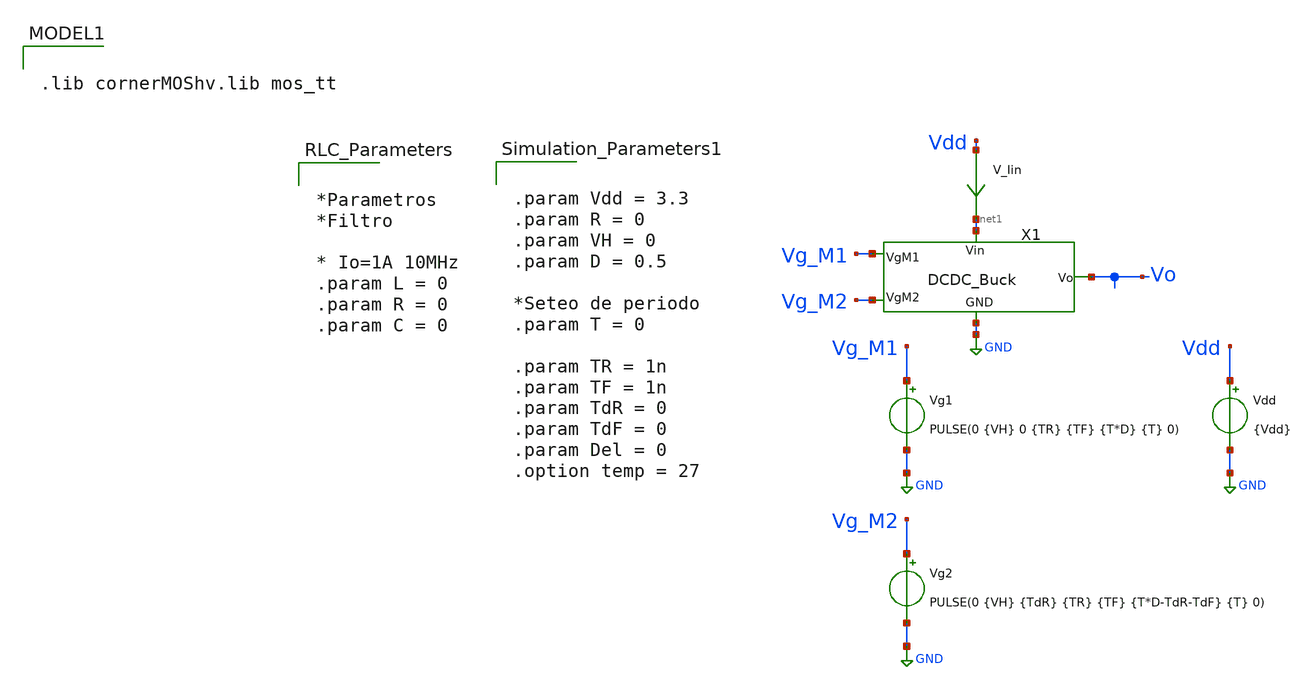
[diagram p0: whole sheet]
** sch_path: ChipUSM_AnalogTrack24/DCDCBuck/TB_DCDCBuck.sch
**.subckt TB_DCDCBuck
Vdd Vdd GND {Vdd}
Vg2 Vg_M2 GND PULSE(0 {VH} {TdR} {TR} {TF} {T*D-TdR-TdF} {T} 0)
Vg1 Vg_M1 GND PULSE(0 {VH} 0 {TR} {TF} {T*D} {T} 0)
V_Iin Vdd net1 0
.save i(v_iin)
X1 Vg_M1 Vg_M2 GND net1 Vo DCDC_Buck
**** begin user architecture code

.lib cornerMOShv.lib mos_tt



*Parametros
*Filtro

* Io=1A 10MHz
.param L = 0
.param R = 0
.param C = 0





.save all  @n.x1.xm1.nsg13_hv_pmos[ids]  @n.x1.xm2.nsg13_hv_nmos[ids]
.param SimTime = 5u

.control
reset
set color0 = white
tran 1n 5u
let Io = i(v.x1.V_Io)
let Id_M1 = @n.x1.xm1.nsg13_hv_pmos[ids]
let Id_M2 = @n.x1.xm2.nsg13_hv_nmos[ids]
let gds_M1 = @n.x1.xm1.nsg13_hv_pmos[gds]
let gds_M2 = @n.x1.xm2.nsg13_hv_nmos[gds]
let Po = Io*v(Vo)
let I_in = i(V_Iin)
let Pin = I_in*v(Vdd)
let Vsd_M1 = v(Vdd) - v(x1.Vc)
let Vds_M2 = v(x1.Vc)
let P_M1 = Vsd_M1*Id_M1
let P_M2 = -Vds_M2*Id_M2
let Ron_M1 = Vsd_M1/Id_M1
let Ron_M2 = Vds_M2/Id_M2
*let Ron_M1 = 1/gds_M1
*let Ron_M2 = 1/gds_M2

let DataMeasBegin = SimTime-1u

meas tran Vo_mean AVG v(Vo) from=2u to=4u
meas tran Io_mean AVG Io from=2u to=4u
meas tran Irms_M1 RMS Id_M1 from=2u to=4u
meas tran Irms_M2 RMS Id_M2 from=2u to=4u
meas tran Po_mean AVG Po from=2u to=4u
meas tran Pin_mean AVG Pin from=2u to=4u
meas tran P_M1_mean AVG P_M1 from=2u to=4u
meas tran P_M2_mean AVG P_M2 from=2u to=4u

let eff = 100*Po_mean/Pin_mean
let loss_M1 = 100*P_M1_mean/Pin_mean
let loss_M2 = 100*P_M2_mean/Pin_mean
let cond_loss_M1 = Irms_M1*Irms_M1*40m*100
let cond_loss_M2 = Irms_M2*Irms_M2*35m*100
let sumaPot = eff+loss_M1+loss_M2
print eff loss_M1 loss_M2 cond_loss_M1 cond_loss_M2 sumaPot

plot Io i(v.x1.V_IL)
plot Id_M1 Id_M2
plot v(Vo)
plot Po Pin
*plot P_M1 P_M2
plot v(x1.Vc)
plot v(Vg_M1) v(Vg_M2)
plot Ron_M1 Ron_M2
write TB_DCDCBuck.raw
.endc



.end




.param temp=27
.param mult_M1 = 1
.param w_M1 =0.3u
.param l_M1 = 0.4u
.param ng_M1 = 1

.param mult_M2 = 1
.param w_M2 =0.3u
.param l_M2 =0.45u
.param ng_M2 =1







.param Vdd = 3.3
.param R = 0
.param VH = 0
.param D = 0.5

*Seteo de periodo
.param T = 0

.param TR = 1n
.param TF = 1n
.param TdR = 0
.param TdF = 0
.param Del = 0
.option temp = 27







**** end user architecture code
**.ends

* expanding   symbol:  ../DCDCBuck/DCDC_Buck.sym # of pins=5
** sym_path: ../DCDCBuck/DCDC_Buck.sym
** sch_path: ../DCDCBuck/DCDC_Buck.sch
.subckt DCDC_Buck VgM1 VgM2 GND Vin Vo
*.iopin Vin
*.ipin VgM1
*.ipin VgM2
*.iopin Vo
*.iopin GND
L1 net2 net1 {L} m=1
C1 net1 GND {C} m=1
V_Io net1 Vo 0
.save i(v_io)
V_IL Vc net2 0
.save i(v_il)
R1 Vo GND {R} m=1
V_IM2 Vc net3 0
.save i(v_im2)
XM3 Vc VgM1 Vin Vin sg13_hv_pmos w={w_M1} l={l_M1} ng={ng_M1} m={mult_M1} mm_ok=1
XM1 GND VgM2 net3 GND sg13_hv_nmos w={w_M2} l={l_M2} ng={ng_M2} m={mult_M2} mm_ok=1
.ends

.GLOBAL GND
.end
